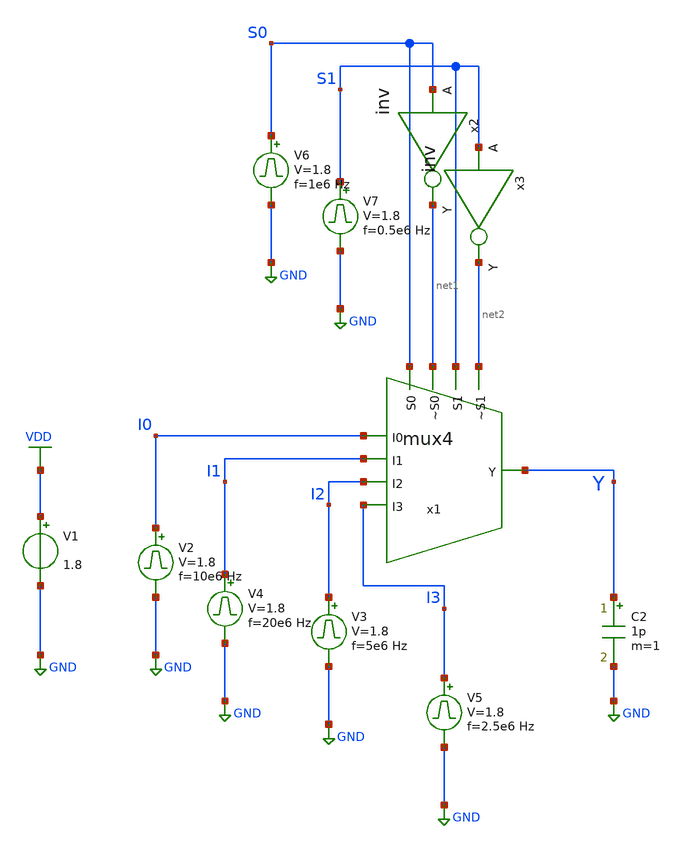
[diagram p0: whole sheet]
** sch_path: circuits/xschem/mux4_tb.sch
**.subckt mux4_tb
V1 VDD GND 1.8
V2 I0 GND pulse 0 1.8 '0.495/ 10e6 ' '0.01/10e6 ' '0.01/10e6 ' '0.49/10e6 ' '1/10e6 '
V3 I2 GND pulse 0 1.8 '0.495/ 5e6 ' '0.01/5e6 ' '0.01/5e6 ' '0.49/5e6 ' '1/5e6 '
C2 Y GND 1p m=1
V4 I1 GND pulse 0 1.8 '0.495/ 20e6 ' '0.01/20e6 ' '0.01/20e6 ' '0.49/20e6 ' '1/20e6 '
x1 S0 net1 S1 net2 I0 I1 Y I2 I3 mux4
V5 I3 GND pulse 0 1.8 '0.495/ 2.5e6 ' '0.01/2.5e6 ' '0.01/2.5e6 ' '0.49/2.5e6 ' '1/2.5e6 '
V6 S0 GND pulse 0 1.8 '0.495/ 1e6 ' '0.01/1e6 ' '0.01/1e6 ' '0.49/1e6 ' '1/1e6 '
V7 S1 GND pulse 0 1.8 '0.495/ 0.5e6 ' '0.01/0.5e6 ' '0.01/0.5e6 ' '0.49/0.5e6 ' '1/0.5e6 '
x2 net1 S0 inv
x3 net2 S1 inv
**** begin user architecture code


.control
save all
tran 1n 4u
plot V(Y) V(S0)+2 V(S1)+4
.endc



** opencircuitdesign pdks install
.lib $::SKYWATER_MODELS/sky130.lib.spice tt


**** end user architecture code
**.ends
.GLOBAL VDD
.GLOBAL GND
.end
